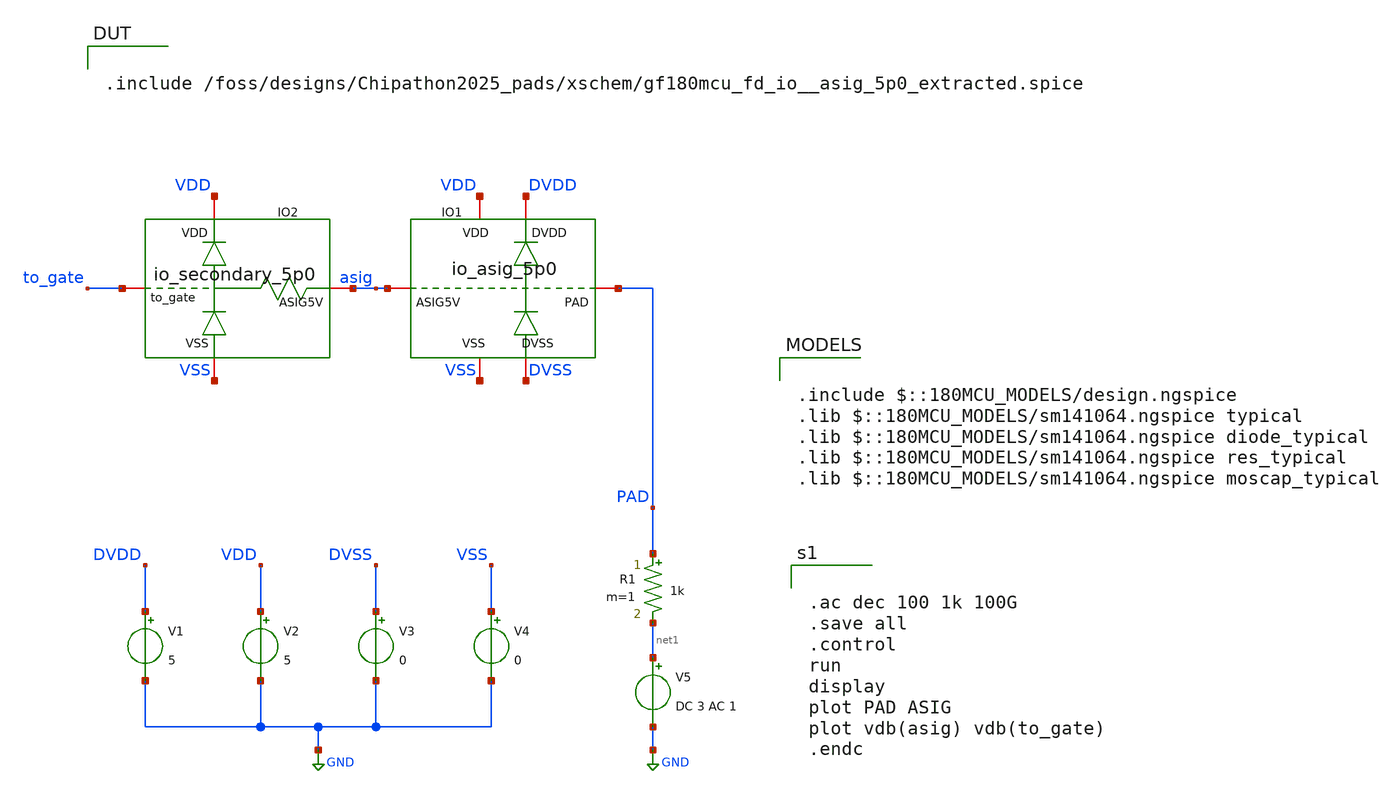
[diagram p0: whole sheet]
** sch_path: examples/pads_simulation/io_secondary_AC_tb.sch
**.subckt io_secondary_AC_tb
V1 DVDD GND 5
V2 VDD GND 5
V3 DVSS GND 0
V4 VSS GND 0
V5 net1 GND DC 3 AC 1
R1 PAD net1 1k m=1
XIO1 DVSS DVDD VSS VDD PAD asig gf180mcu_fd_io__asig_5p0_extracted
XIO2 VDD to_gate asig VSS io_secondary_5p0
**** begin user architecture code

.include /foss/designs/Chipathon2025_pads/xschem/gf180mcu_fd_io__asig_5p0_extracted.spice


.include $::180MCU_MODELS/design.ngspice
.lib $::180MCU_MODELS/sm141064.ngspice typical
.lib $::180MCU_MODELS/sm141064.ngspice diode_typical
.lib $::180MCU_MODELS/sm141064.ngspice res_typical
.lib $::180MCU_MODELS/sm141064.ngspice moscap_typical



.ac dec 100 1k 100G
.save all
.control
run
display
plot PAD ASIG
plot vdb(asig) vdb(to_gate)
.endc


**** end user architecture code
**.ends
.GLOBAL GND
.end
